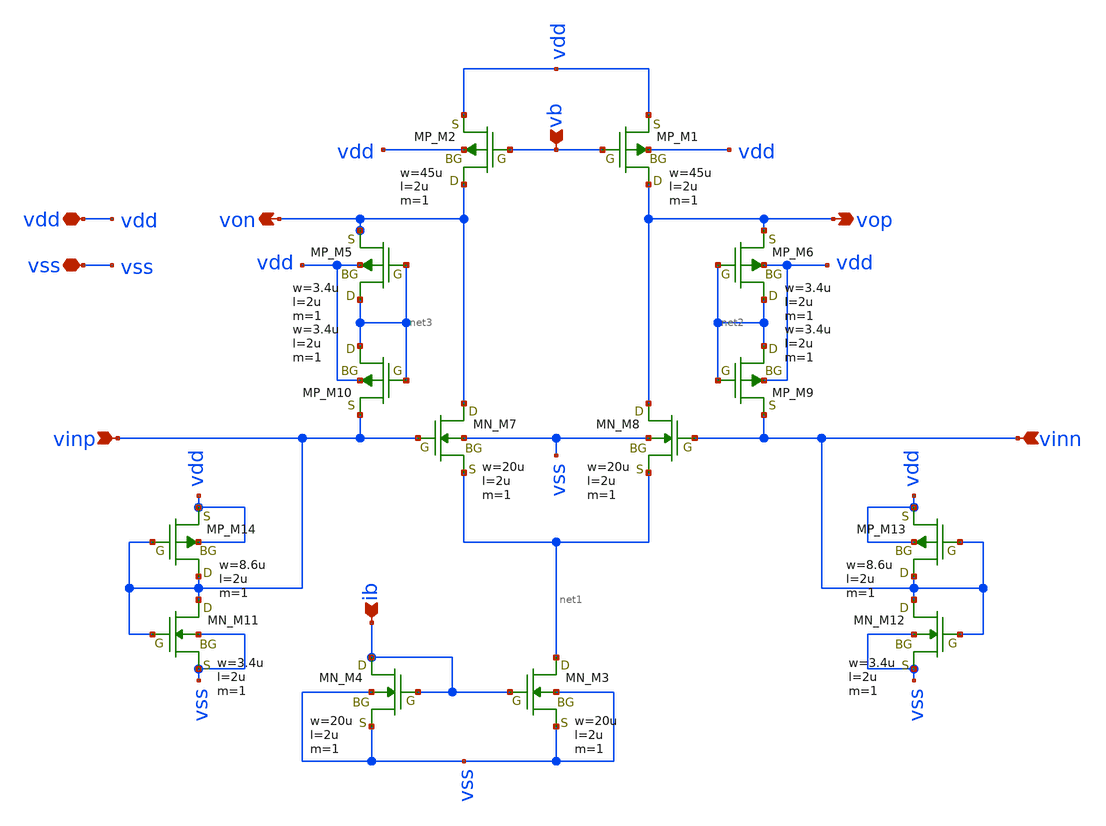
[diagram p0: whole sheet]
** sch_path: member_project/JJY_Receiver/Masahiro/jjy_recv/diff_amp/fully_diff_amp.sch
**.subckt fully_diff_amp vop von vinp vb ib vinn vdd vss
*.opin vop
*.opin von
*.ipin vinp
*.ipin vb
*.ipin ib
*.ipin vinn
*.iopin vdd
*.iopin vss
XM1 vop vb vdd vdd PMOS w=45u l=2u as=0 ad=0 ps=0 pd=0 nrd=0 nrs=0 m=1
XM2 von vb vdd vdd PMOS w=45u l=2u as=0 ad=0 ps=0 pd=0 nrd=0 nrs=0 m=1
XM3 net1 ib vss vss NMOS w=20u l=2u as=0 ad=0 ps=0 pd=0 nrd=0 nrs=0 m=1
XM4 ib ib vss vss NMOS w=20u l=2u as=0 ad=0 ps=0 pd=0 nrd=0 nrs=0 m=1
XM7 von vinp net1 vss NMOS w=20u l=2u as=0 ad=0 ps=0 pd=0 nrd=0 nrs=0 m=1
XM8 vop vinn net1 vss NMOS w=20u l=2u as=0 ad=0 ps=0 pd=0 nrd=0 nrs=0 m=1
XM6 net2 net2 vop vdd PMOS w=3.4u l=2u as=0 ad=0 ps=0 pd=0 nrd=0 nrs=0 m=1
XM9 net2 net2 vinn vdd PMOS w=3.4u l=2u as=0 ad=0 ps=0 pd=0 nrd=0 nrs=0 m=1
XM5 net3 net3 von vdd PMOS w=3.4u l=2u as=0 ad=0 ps=0 pd=0 nrd=0 nrs=0 m=1
XM10 net3 net3 vinp vdd PMOS w=3.4u l=2u as=0 ad=0 ps=0 pd=0 nrd=0 nrs=0 m=1
XM12 vinn vinn vss vss NMOS w=3.4u l=2u as=0 ad=0 ps=0 pd=0 nrd=0 nrs=0 m=1
XM13 vinn vinn vdd vdd PMOS w=8.6u l=2u as=0 ad=0 ps=0 pd=0 nrd=0 nrs=0 m=1
XM11 vinp vinp vss vss NMOS w=3.4u l=2u as=0 ad=0 ps=0 pd=0 nrd=0 nrs=0 m=1
XM14 vinp vinp vdd vdd PMOS w=8.6u l=2u as=0 ad=0 ps=0 pd=0 nrd=0 nrs=0 m=1
**** begin user architecture code
 .include $::LIB/ip62_models
**** end user architecture code
**.ends
.end
